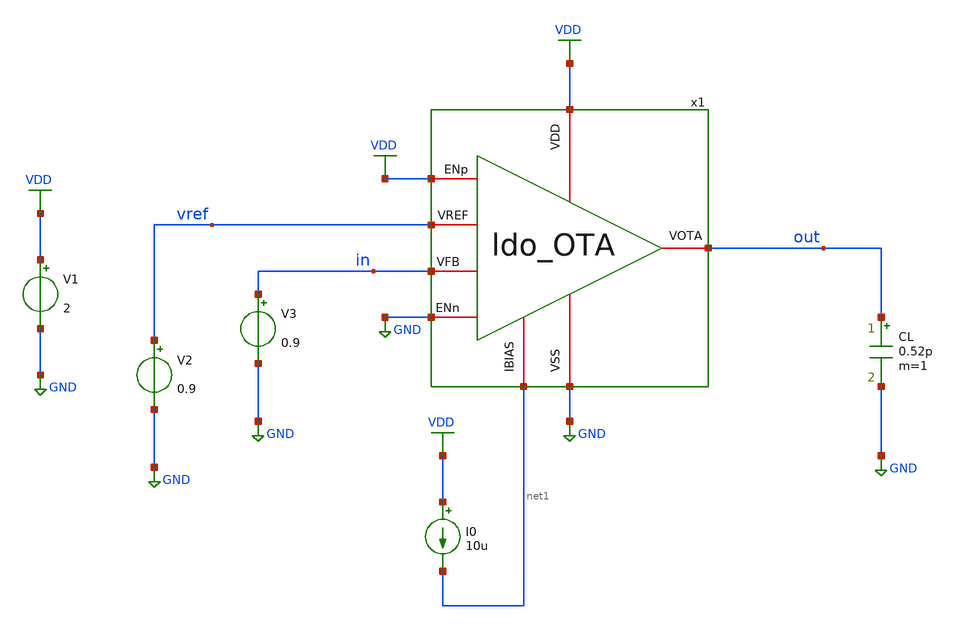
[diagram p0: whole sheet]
** sch_path: designs/libs/tb_ldo/tb_ldo_OTA_tran/tb_ldo_OTA_tran.sch
**.subckt tb_ldo_OTA_tran
V1 VDD GND 2
V2 vref GND 0.9
I0 VDD net1 10u
CL out GND 0.52p m=1
V3 in GND 0.9
x1 VDD vref in out net1 GND VDD GND ldo_OTA
**** begin user architecture code

.include $::180MCU_MODELS/design.ngspice
.lib $::180MCU_MODELS/sm141064.ngspice typical
.lib $::180MCU_MODELS/sm141064.ngspice cap_mim
.lib $::180MCU_MODELS/sm141064.ngspice moscap_typical
.lib $::180MCU_MODELS/sm141064.ngspice mimcap_typical
.lib $::180MCU_MODELS/sm141064.ngspice res_typical
* .lib $::180MCU_MODELS/sm141064.ngspice res_statistical
* ngspice commands




.control
save all

** Define input signal
let fsig = 1k
let tper = 1/fsig
let tfr = 0.01*tper
let ton = 0.5*tper-2*tfr

** Define transient params
let tstop = 2*tper
let tstep = 0.001*tper

** Set sources
alter @V3[PULSE] = [ 0.91 0.89 0 $&tfr $&tfr $&ton $&tper 0]

** Simulations
tran $&tstep $&tstop

** Plots
setplot tran1
let vout = v(out)
let vin = v(in)
plot vin
plot vout

write tb_ldo_OTA_tran.raw

.endc
* ngspice commands



**** end user architecture code
**.ends

* expanding   symbol:  libs/core_ldo/ldo_OTA/ldo_OTA.sym # of pins=8
** sym_path: designs/libs/core_ldo/ldo_OTA/ldo_OTA.sym
** sch_path: designs/libs/core_ldo/ldo_OTA/ldo_OTA.sch
.subckt ldo_OTA VDD VREF VFB VOTA IBIAS VSS ENp ENn
*.iopin VDD
*.iopin VSS
*.iopin VOTA
*.iopin VREF
*.iopin IBIAS
*.iopin VFB
*.ipin ENp
*.ipin ENn
XM3 Vbp1 Vbp1 VDD VDD pfet_05v0 L=1.00u W=5.50u nf=1 ad='int((nf+1)/2) * W/nf * 0.18u' as='int((nf+2)/2) * W/nf * 0.18u'
+ pd='2*int((nf+1)/2) * (W/nf + 0.18u)' ps='2*int((nf+2)/2) * (W/nf + 0.18u)' nrd='0.18u / W' nrs='0.18u / W'
+ sa=0 sb=0 sd=0 m=2
XM4 Vbp2 Vbp2 VDD VDD pfet_05v0 L=1.00u W=5.50u nf=1 ad='int((nf+1)/2) * W/nf * 0.18u' as='int((nf+2)/2) * W/nf * 0.18u'
+ pd='2*int((nf+1)/2) * (W/nf + 0.18u)' ps='2*int((nf+2)/2) * (W/nf + 0.18u)' nrd='0.18u / W' nrs='0.18u / W'
+ sa=0 sb=0 sd=0 m=2
XM5 Vbn2 Vbp1 VDD VDD pfet_05v0 L=1.00u W=5.50u nf=1 ad='int((nf+1)/2) * W/nf * 0.18u' as='int((nf+2)/2) * W/nf * 0.18u'
+ pd='2*int((nf+1)/2) * (W/nf + 0.18u)' ps='2*int((nf+2)/2) * (W/nf + 0.18u)' nrd='0.18u / W' nrs='0.18u / W'
+ sa=0 sb=0 sd=0 m=2
XM6 VOTA Vbp2 VDD VDD pfet_05v0 L=1.00u W=5.50u nf=1 ad='int((nf+1)/2) * W/nf * 0.18u' as='int((nf+2)/2) * W/nf * 0.18u'
+ pd='2*int((nf+1)/2) * (W/nf + 0.18u)' ps='2*int((nf+2)/2) * (W/nf + 0.18u)' nrd='0.18u / W' nrs='0.18u / W'
+ sa=0 sb=0 sd=0 m=6
XM9 Vbn1 Vbn1 VSS VSS nfet_05v0 L=1.00u W=3.00u nf=1 ad='int((nf+1)/2) * W/nf * 0.18u' as='int((nf+2)/2) * W/nf * 0.18u'
+ pd='2*int((nf+1)/2) * (W/nf + 0.18u)' ps='2*int((nf+2)/2) * (W/nf + 0.18u)' nrd='0.18u / W' nrs='0.18u / W'
+ sa=0 sb=0 sd=0 m=2
XM10 Vtail Vbn1 VSS VSS nfet_05v0 L=1.00u W=3.00u nf=1 ad='int((nf+1)/2) * W/nf * 0.18u' as='int((nf+2)/2) * W/nf * 0.18u'
+ pd='2*int((nf+1)/2) * (W/nf + 0.18u)' ps='2*int((nf+2)/2) * (W/nf + 0.18u)' nrd='0.18u / W' nrs='0.18u / W'
+ sa=0 sb=0 sd=0 m=2
XM7 Vbn2 Vbn2 VSS VSS nfet_05v0 L=1.00u W=1.25u nf=1 ad='int((nf+1)/2) * W/nf * 0.18u' as='int((nf+2)/2) * W/nf * 0.18u'
+ pd='2*int((nf+1)/2) * (W/nf + 0.18u)' ps='2*int((nf+2)/2) * (W/nf + 0.18u)' nrd='0.18u / W' nrs='0.18u / W'
+ sa=0 sb=0 sd=0 m=2
XM8 VOTA Vbn2 VSS VSS nfet_05v0 L=1.00u W=1.25u nf=1 ad='int((nf+1)/2) * W/nf * 0.18u' as='int((nf+2)/2) * W/nf * 0.18u'
+ pd='2*int((nf+1)/2) * (W/nf + 0.18u)' ps='2*int((nf+2)/2) * (W/nf + 0.18u)' nrd='0.18u / W' nrs='0.18u / W'
+ sa=0 sb=0 sd=0 m=6
XM1 Vbp1 VREF Vtail VSS nfet_05v0 L=0.60u W=5.00u nf=1 ad='int((nf+1)/2) * W/nf * 0.18u' as='int((nf+2)/2) * W/nf * 0.18u'
+ pd='2*int((nf+1)/2) * (W/nf + 0.18u)' ps='2*int((nf+2)/2) * (W/nf + 0.18u)' nrd='0.18u / W' nrs='0.18u / W'
+ sa=0 sb=0 sd=0 m=14
XM2 Vbp2 VFB Vtail VSS nfet_05v0 L=0.60u W=5.00u nf=1 ad='int((nf+1)/2) * W/nf * 0.18u' as='int((nf+2)/2) * W/nf * 0.18u'
+ pd='2*int((nf+1)/2) * (W/nf + 0.18u)' ps='2*int((nf+2)/2) * (W/nf + 0.18u)' nrd='0.18u / W' nrs='0.18u / W'
+ sa=0 sb=0 sd=0 m=14
XMpota_dummy_L[3] VDD VDD VDD VDD pfet_05v0 L=1.00u W=5.50u nf=1 ad='int((nf+1)/2) * W/nf * 0.18u' as='int((nf+2)/2) * W/nf * 0.18u'
+ pd='2*int((nf+1)/2) * (W/nf + 0.18u)' ps='2*int((nf+2)/2) * (W/nf + 0.18u)' nrd='0.18u / W' nrs='0.18u / W'
+ sa=0 sb=0 sd=0 m=1
XMpota_dummy_L[2] VDD VDD VDD VDD pfet_05v0 L=1.00u W=5.50u nf=1 ad='int((nf+1)/2) * W/nf * 0.18u' as='int((nf+2)/2) * W/nf * 0.18u'
+ pd='2*int((nf+1)/2) * (W/nf + 0.18u)' ps='2*int((nf+2)/2) * (W/nf + 0.18u)' nrd='0.18u / W' nrs='0.18u / W'
+ sa=0 sb=0 sd=0 m=1
XMpota_dummy_L[1] VDD VDD VDD VDD pfet_05v0 L=1.00u W=5.50u nf=1 ad='int((nf+1)/2) * W/nf * 0.18u' as='int((nf+2)/2) * W/nf * 0.18u'
+ pd='2*int((nf+1)/2) * (W/nf + 0.18u)' ps='2*int((nf+2)/2) * (W/nf + 0.18u)' nrd='0.18u / W' nrs='0.18u / W'
+ sa=0 sb=0 sd=0 m=1
XMpota_dummy_L[0] VDD VDD VDD VDD pfet_05v0 L=1.00u W=5.50u nf=1 ad='int((nf+1)/2) * W/nf * 0.18u' as='int((nf+2)/2) * W/nf * 0.18u'
+ pd='2*int((nf+1)/2) * (W/nf + 0.18u)' ps='2*int((nf+2)/2) * (W/nf + 0.18u)' nrd='0.18u / W' nrs='0.18u / W'
+ sa=0 sb=0 sd=0 m=1
XMpota_dummy_TB[15] VDD VDD VDD VDD pfet_05v0 L=1.00u W=5.50u nf=1 ad='int((nf+1)/2) * W/nf * 0.18u'
+ as='int((nf+2)/2) * W/nf * 0.18u' pd='2*int((nf+1)/2) * (W/nf + 0.18u)' ps='2*int((nf+2)/2) * (W/nf + 0.18u)'
+ nrd='0.18u / W' nrs='0.18u / W' sa=0 sb=0 sd=0 m=1
XMpota_dummy_TB[14] VDD VDD VDD VDD pfet_05v0 L=1.00u W=5.50u nf=1 ad='int((nf+1)/2) * W/nf * 0.18u'
+ as='int((nf+2)/2) * W/nf * 0.18u' pd='2*int((nf+1)/2) * (W/nf + 0.18u)' ps='2*int((nf+2)/2) * (W/nf + 0.18u)'
+ nrd='0.18u / W' nrs='0.18u / W' sa=0 sb=0 sd=0 m=1
XMpota_dummy_TB[13] VDD VDD VDD VDD pfet_05v0 L=1.00u W=5.50u nf=1 ad='int((nf+1)/2) * W/nf * 0.18u'
+ as='int((nf+2)/2) * W/nf * 0.18u' pd='2*int((nf+1)/2) * (W/nf + 0.18u)' ps='2*int((nf+2)/2) * (W/nf + 0.18u)'
+ nrd='0.18u / W' nrs='0.18u / W' sa=0 sb=0 sd=0 m=1
XMpota_dummy_TB[12] VDD VDD VDD VDD pfet_05v0 L=1.00u W=5.50u nf=1 ad='int((nf+1)/2) * W/nf * 0.18u'
+ as='int((nf+2)/2) * W/nf * 0.18u' pd='2*int((nf+1)/2) * (W/nf + 0.18u)' ps='2*int((nf+2)/2) * (W/nf + 0.18u)'
+ nrd='0.18u / W' nrs='0.18u / W' sa=0 sb=0 sd=0 m=1
XMpota_dummy_TB[11] VDD VDD VDD VDD pfet_05v0 L=1.00u W=5.50u nf=1 ad='int((nf+1)/2) * W/nf * 0.18u'
+ as='int((nf+2)/2) * W/nf * 0.18u' pd='2*int((nf+1)/2) * (W/nf + 0.18u)' ps='2*int((nf+2)/2) * (W/nf + 0.18u)'
+ nrd='0.18u / W' nrs='0.18u / W' sa=0 sb=0 sd=0 m=1
XMpota_dummy_TB[10] VDD VDD VDD VDD pfet_05v0 L=1.00u W=5.50u nf=1 ad='int((nf+1)/2) * W/nf * 0.18u'
+ as='int((nf+2)/2) * W/nf * 0.18u' pd='2*int((nf+1)/2) * (W/nf + 0.18u)' ps='2*int((nf+2)/2) * (W/nf + 0.18u)'
+ nrd='0.18u / W' nrs='0.18u / W' sa=0 sb=0 sd=0 m=1
XMpota_dummy_TB[9] VDD VDD VDD VDD pfet_05v0 L=1.00u W=5.50u nf=1 ad='int((nf+1)/2) * W/nf * 0.18u' as='int((nf+2)/2) * W/nf * 0.18u'
+ pd='2*int((nf+1)/2) * (W/nf + 0.18u)' ps='2*int((nf+2)/2) * (W/nf + 0.18u)' nrd='0.18u / W' nrs='0.18u / W'
+ sa=0 sb=0 sd=0 m=1
XMpota_dummy_TB[8] VDD VDD VDD VDD pfet_05v0 L=1.00u W=5.50u nf=1 ad='int((nf+1)/2) * W/nf * 0.18u' as='int((nf+2)/2) * W/nf * 0.18u'
+ pd='2*int((nf+1)/2) * (W/nf + 0.18u)' ps='2*int((nf+2)/2) * (W/nf + 0.18u)' nrd='0.18u / W' nrs='0.18u / W'
+ sa=0 sb=0 sd=0 m=1
XMpota_dummy_TB[7] VDD VDD VDD VDD pfet_05v0 L=1.00u W=5.50u nf=1 ad='int((nf+1)/2) * W/nf * 0.18u' as='int((nf+2)/2) * W/nf * 0.18u'
+ pd='2*int((nf+1)/2) * (W/nf + 0.18u)' ps='2*int((nf+2)/2) * (W/nf + 0.18u)' nrd='0.18u / W' nrs='0.18u / W'
+ sa=0 sb=0 sd=0 m=1
XMpota_dummy_TB[6] VDD VDD VDD VDD pfet_05v0 L=1.00u W=5.50u nf=1 ad='int((nf+1)/2) * W/nf * 0.18u' as='int((nf+2)/2) * W/nf * 0.18u'
+ pd='2*int((nf+1)/2) * (W/nf + 0.18u)' ps='2*int((nf+2)/2) * (W/nf + 0.18u)' nrd='0.18u / W' nrs='0.18u / W'
+ sa=0 sb=0 sd=0 m=1
XMpota_dummy_TB[5] VDD VDD VDD VDD pfet_05v0 L=1.00u W=5.50u nf=1 ad='int((nf+1)/2) * W/nf * 0.18u' as='int((nf+2)/2) * W/nf * 0.18u'
+ pd='2*int((nf+1)/2) * (W/nf + 0.18u)' ps='2*int((nf+2)/2) * (W/nf + 0.18u)' nrd='0.18u / W' nrs='0.18u / W'
+ sa=0 sb=0 sd=0 m=1
XMpota_dummy_TB[4] VDD VDD VDD VDD pfet_05v0 L=1.00u W=5.50u nf=1 ad='int((nf+1)/2) * W/nf * 0.18u' as='int((nf+2)/2) * W/nf * 0.18u'
+ pd='2*int((nf+1)/2) * (W/nf + 0.18u)' ps='2*int((nf+2)/2) * (W/nf + 0.18u)' nrd='0.18u / W' nrs='0.18u / W'
+ sa=0 sb=0 sd=0 m=1
XMpota_dummy_TB[3] VDD VDD VDD VDD pfet_05v0 L=1.00u W=5.50u nf=1 ad='int((nf+1)/2) * W/nf * 0.18u' as='int((nf+2)/2) * W/nf * 0.18u'
+ pd='2*int((nf+1)/2) * (W/nf + 0.18u)' ps='2*int((nf+2)/2) * (W/nf + 0.18u)' nrd='0.18u / W' nrs='0.18u / W'
+ sa=0 sb=0 sd=0 m=1
XMpota_dummy_TB[2] VDD VDD VDD VDD pfet_05v0 L=1.00u W=5.50u nf=1 ad='int((nf+1)/2) * W/nf * 0.18u' as='int((nf+2)/2) * W/nf * 0.18u'
+ pd='2*int((nf+1)/2) * (W/nf + 0.18u)' ps='2*int((nf+2)/2) * (W/nf + 0.18u)' nrd='0.18u / W' nrs='0.18u / W'
+ sa=0 sb=0 sd=0 m=1
XMpota_dummy_TB[1] VDD VDD VDD VDD pfet_05v0 L=1.00u W=5.50u nf=1 ad='int((nf+1)/2) * W/nf * 0.18u' as='int((nf+2)/2) * W/nf * 0.18u'
+ pd='2*int((nf+1)/2) * (W/nf + 0.18u)' ps='2*int((nf+2)/2) * (W/nf + 0.18u)' nrd='0.18u / W' nrs='0.18u / W'
+ sa=0 sb=0 sd=0 m=1
XMpota_dummy_TB[0] VDD VDD VDD VDD pfet_05v0 L=1.00u W=5.50u nf=1 ad='int((nf+1)/2) * W/nf * 0.18u' as='int((nf+2)/2) * W/nf * 0.18u'
+ pd='2*int((nf+1)/2) * (W/nf + 0.18u)' ps='2*int((nf+2)/2) * (W/nf + 0.18u)' nrd='0.18u / W' nrs='0.18u / W'
+ sa=0 sb=0 sd=0 m=1
XMndiff_dummy_L[7] VSS VSS VSS VSS nfet_05v0 L=0.60u W=5.00u nf=1 ad='int((nf+1)/2) * W/nf * 0.18u' as='int((nf+2)/2) * W/nf * 0.18u'
+ pd='2*int((nf+1)/2) * (W/nf + 0.18u)' ps='2*int((nf+2)/2) * (W/nf + 0.18u)' nrd='0.18u / W' nrs='0.18u / W'
+ sa=0 sb=0 sd=0 m=1
XMndiff_dummy_L[6] VSS VSS VSS VSS nfet_05v0 L=0.60u W=5.00u nf=1 ad='int((nf+1)/2) * W/nf * 0.18u' as='int((nf+2)/2) * W/nf * 0.18u'
+ pd='2*int((nf+1)/2) * (W/nf + 0.18u)' ps='2*int((nf+2)/2) * (W/nf + 0.18u)' nrd='0.18u / W' nrs='0.18u / W'
+ sa=0 sb=0 sd=0 m=1
XMndiff_dummy_L[5] VSS VSS VSS VSS nfet_05v0 L=0.60u W=5.00u nf=1 ad='int((nf+1)/2) * W/nf * 0.18u' as='int((nf+2)/2) * W/nf * 0.18u'
+ pd='2*int((nf+1)/2) * (W/nf + 0.18u)' ps='2*int((nf+2)/2) * (W/nf + 0.18u)' nrd='0.18u / W' nrs='0.18u / W'
+ sa=0 sb=0 sd=0 m=1
XMndiff_dummy_L[4] VSS VSS VSS VSS nfet_05v0 L=0.60u W=5.00u nf=1 ad='int((nf+1)/2) * W/nf * 0.18u' as='int((nf+2)/2) * W/nf * 0.18u'
+ pd='2*int((nf+1)/2) * (W/nf + 0.18u)' ps='2*int((nf+2)/2) * (W/nf + 0.18u)' nrd='0.18u / W' nrs='0.18u / W'
+ sa=0 sb=0 sd=0 m=1
XMndiff_dummy_L[3] VSS VSS VSS VSS nfet_05v0 L=0.60u W=5.00u nf=1 ad='int((nf+1)/2) * W/nf * 0.18u' as='int((nf+2)/2) * W/nf * 0.18u'
+ pd='2*int((nf+1)/2) * (W/nf + 0.18u)' ps='2*int((nf+2)/2) * (W/nf + 0.18u)' nrd='0.18u / W' nrs='0.18u / W'
+ sa=0 sb=0 sd=0 m=1
XMndiff_dummy_L[2] VSS VSS VSS VSS nfet_05v0 L=0.60u W=5.00u nf=1 ad='int((nf+1)/2) * W/nf * 0.18u' as='int((nf+2)/2) * W/nf * 0.18u'
+ pd='2*int((nf+1)/2) * (W/nf + 0.18u)' ps='2*int((nf+2)/2) * (W/nf + 0.18u)' nrd='0.18u / W' nrs='0.18u / W'
+ sa=0 sb=0 sd=0 m=1
XMndiff_dummy_L[1] VSS VSS VSS VSS nfet_05v0 L=0.60u W=5.00u nf=1 ad='int((nf+1)/2) * W/nf * 0.18u' as='int((nf+2)/2) * W/nf * 0.18u'
+ pd='2*int((nf+1)/2) * (W/nf + 0.18u)' ps='2*int((nf+2)/2) * (W/nf + 0.18u)' nrd='0.18u / W' nrs='0.18u / W'
+ sa=0 sb=0 sd=0 m=1
XMndiff_dummy_L[0] VSS VSS VSS VSS nfet_05v0 L=0.60u W=5.00u nf=1 ad='int((nf+1)/2) * W/nf * 0.18u' as='int((nf+2)/2) * W/nf * 0.18u'
+ pd='2*int((nf+1)/2) * (W/nf + 0.18u)' ps='2*int((nf+2)/2) * (W/nf + 0.18u)' nrd='0.18u / W' nrs='0.18u / W'
+ sa=0 sb=0 sd=0 m=1
XMndiff_dummy_TB[17] VSS VSS VSS VSS nfet_05v0 L=0.60u W=5.00u nf=1 ad='int((nf+1)/2) * W/nf * 0.18u'
+ as='int((nf+2)/2) * W/nf * 0.18u' pd='2*int((nf+1)/2) * (W/nf + 0.18u)' ps='2*int((nf+2)/2) * (W/nf + 0.18u)'
+ nrd='0.18u / W' nrs='0.18u / W' sa=0 sb=0 sd=0 m=1
XMndiff_dummy_TB[16] VSS VSS VSS VSS nfet_05v0 L=0.60u W=5.00u nf=1 ad='int((nf+1)/2) * W/nf * 0.18u'
+ as='int((nf+2)/2) * W/nf * 0.18u' pd='2*int((nf+1)/2) * (W/nf + 0.18u)' ps='2*int((nf+2)/2) * (W/nf + 0.18u)'
+ nrd='0.18u / W' nrs='0.18u / W' sa=0 sb=0 sd=0 m=1
XMndiff_dummy_TB[15] VSS VSS VSS VSS nfet_05v0 L=0.60u W=5.00u nf=1 ad='int((nf+1)/2) * W/nf * 0.18u'
+ as='int((nf+2)/2) * W/nf * 0.18u' pd='2*int((nf+1)/2) * (W/nf + 0.18u)' ps='2*int((nf+2)/2) * (W/nf + 0.18u)'
+ nrd='0.18u / W' nrs='0.18u / W' sa=0 sb=0 sd=0 m=1
XMndiff_dummy_TB[14] VSS VSS VSS VSS nfet_05v0 L=0.60u W=5.00u nf=1 ad='int((nf+1)/2) * W/nf * 0.18u'
+ as='int((nf+2)/2) * W/nf * 0.18u' pd='2*int((nf+1)/2) * (W/nf + 0.18u)' ps='2*int((nf+2)/2) * (W/nf + 0.18u)'
+ nrd='0.18u / W' nrs='0.18u / W' sa=0 sb=0 sd=0 m=1
XMndiff_dummy_TB[13] VSS VSS VSS VSS nfet_05v0 L=0.60u W=5.00u nf=1 ad='int((nf+1)/2) * W/nf * 0.18u'
+ as='int((nf+2)/2) * W/nf * 0.18u' pd='2*int((nf+1)/2) * (W/nf + 0.18u)' ps='2*int((nf+2)/2) * (W/nf + 0.18u)'
+ nrd='0.18u / W' nrs='0.18u / W' sa=0 sb=0 sd=0 m=1
XMndiff_dummy_TB[12] VSS VSS VSS VSS nfet_05v0 L=0.60u W=5.00u nf=1 ad='int((nf+1)/2) * W/nf * 0.18u'
+ as='int((nf+2)/2) * W/nf * 0.18u' pd='2*int((nf+1)/2) * (W/nf + 0.18u)' ps='2*int((nf+2)/2) * (W/nf + 0.18u)'
+ nrd='0.18u / W' nrs='0.18u / W' sa=0 sb=0 sd=0 m=1
XMndiff_dummy_TB[11] VSS VSS VSS VSS nfet_05v0 L=0.60u W=5.00u nf=1 ad='int((nf+1)/2) * W/nf * 0.18u'
+ as='int((nf+2)/2) * W/nf * 0.18u' pd='2*int((nf+1)/2) * (W/nf + 0.18u)' ps='2*int((nf+2)/2) * (W/nf + 0.18u)'
+ nrd='0.18u / W' nrs='0.18u / W' sa=0 sb=0 sd=0 m=1
XMndiff_dummy_TB[10] VSS VSS VSS VSS nfet_05v0 L=0.60u W=5.00u nf=1 ad='int((nf+1)/2) * W/nf * 0.18u'
+ as='int((nf+2)/2) * W/nf * 0.18u' pd='2*int((nf+1)/2) * (W/nf + 0.18u)' ps='2*int((nf+2)/2) * (W/nf + 0.18u)'
+ nrd='0.18u / W' nrs='0.18u / W' sa=0 sb=0 sd=0 m=1
XMndiff_dummy_TB[9] VSS VSS VSS VSS nfet_05v0 L=0.60u W=5.00u nf=1 ad='int((nf+1)/2) * W/nf * 0.18u'
+ as='int((nf+2)/2) * W/nf * 0.18u' pd='2*int((nf+1)/2) * (W/nf + 0.18u)' ps='2*int((nf+2)/2) * (W/nf + 0.18u)'
+ nrd='0.18u / W' nrs='0.18u / W' sa=0 sb=0 sd=0 m=1
XMndiff_dummy_TB[8] VSS VSS VSS VSS nfet_05v0 L=0.60u W=5.00u nf=1 ad='int((nf+1)/2) * W/nf * 0.18u'
+ as='int((nf+2)/2) * W/nf * 0.18u' pd='2*int((nf+1)/2) * (W/nf + 0.18u)' ps='2*int((nf+2)/2) * (W/nf + 0.18u)'
+ nrd='0.18u / W' nrs='0.18u / W' sa=0 sb=0 sd=0 m=1
XMndiff_dummy_TB[7] VSS VSS VSS VSS nfet_05v0 L=0.60u W=5.00u nf=1 ad='int((nf+1)/2) * W/nf * 0.18u'
+ as='int((nf+2)/2) * W/nf * 0.18u' pd='2*int((nf+1)/2) * (W/nf + 0.18u)' ps='2*int((nf+2)/2) * (W/nf + 0.18u)'
+ nrd='0.18u / W' nrs='0.18u / W' sa=0 sb=0 sd=0 m=1
XMndiff_dummy_TB[6] VSS VSS VSS VSS nfet_05v0 L=0.60u W=5.00u nf=1 ad='int((nf+1)/2) * W/nf * 0.18u'
+ as='int((nf+2)/2) * W/nf * 0.18u' pd='2*int((nf+1)/2) * (W/nf + 0.18u)' ps='2*int((nf+2)/2) * (W/nf + 0.18u)'
+ nrd='0.18u / W' nrs='0.18u / W' sa=0 sb=0 sd=0 m=1
XMndiff_dummy_TB[5] VSS VSS VSS VSS nfet_05v0 L=0.60u W=5.00u nf=1 ad='int((nf+1)/2) * W/nf * 0.18u'
+ as='int((nf+2)/2) * W/nf * 0.18u' pd='2*int((nf+1)/2) * (W/nf + 0.18u)' ps='2*int((nf+2)/2) * (W/nf + 0.18u)'
+ nrd='0.18u / W' nrs='0.18u / W' sa=0 sb=0 sd=0 m=1
XMndiff_dummy_TB[4] VSS VSS VSS VSS nfet_05v0 L=0.60u W=5.00u nf=1 ad='int((nf+1)/2) * W/nf * 0.18u'
+ as='int((nf+2)/2) * W/nf * 0.18u' pd='2*int((nf+1)/2) * (W/nf + 0.18u)' ps='2*int((nf+2)/2) * (W/nf + 0.18u)'
+ nrd='0.18u / W' nrs='0.18u / W' sa=0 sb=0 sd=0 m=1
XMndiff_dummy_TB[3] VSS VSS VSS VSS nfet_05v0 L=0.60u W=5.00u nf=1 ad='int((nf+1)/2) * W/nf * 0.18u'
+ as='int((nf+2)/2) * W/nf * 0.18u' pd='2*int((nf+1)/2) * (W/nf + 0.18u)' ps='2*int((nf+2)/2) * (W/nf + 0.18u)'
+ nrd='0.18u / W' nrs='0.18u / W' sa=0 sb=0 sd=0 m=1
XMndiff_dummy_TB[2] VSS VSS VSS VSS nfet_05v0 L=0.60u W=5.00u nf=1 ad='int((nf+1)/2) * W/nf * 0.18u'
+ as='int((nf+2)/2) * W/nf * 0.18u' pd='2*int((nf+1)/2) * (W/nf + 0.18u)' ps='2*int((nf+2)/2) * (W/nf + 0.18u)'
+ nrd='0.18u / W' nrs='0.18u / W' sa=0 sb=0 sd=0 m=1
XMndiff_dummy_TB[1] VSS VSS VSS VSS nfet_05v0 L=0.60u W=5.00u nf=1 ad='int((nf+1)/2) * W/nf * 0.18u'
+ as='int((nf+2)/2) * W/nf * 0.18u' pd='2*int((nf+1)/2) * (W/nf + 0.18u)' ps='2*int((nf+2)/2) * (W/nf + 0.18u)'
+ nrd='0.18u / W' nrs='0.18u / W' sa=0 sb=0 sd=0 m=1
XMndiff_dummy_TB[0] VSS VSS VSS VSS nfet_05v0 L=0.60u W=5.00u nf=1 ad='int((nf+1)/2) * W/nf * 0.18u'
+ as='int((nf+2)/2) * W/nf * 0.18u' pd='2*int((nf+1)/2) * (W/nf + 0.18u)' ps='2*int((nf+2)/2) * (W/nf + 0.18u)'
+ nrd='0.18u / W' nrs='0.18u / W' sa=0 sb=0 sd=0 m=1
XMnota_dummy_L[3] VSS VSS VSS VSS nfet_05v0 L=1.00u W=1.25u nf=1 ad='int((nf+1)/2) * W/nf * 0.18u' as='int((nf+2)/2) * W/nf * 0.18u'
+ pd='2*int((nf+1)/2) * (W/nf + 0.18u)' ps='2*int((nf+2)/2) * (W/nf + 0.18u)' nrd='0.18u / W' nrs='0.18u / W'
+ sa=0 sb=0 sd=0 m=1
XMnota_dummy_L[2] VSS VSS VSS VSS nfet_05v0 L=1.00u W=1.25u nf=1 ad='int((nf+1)/2) * W/nf * 0.18u' as='int((nf+2)/2) * W/nf * 0.18u'
+ pd='2*int((nf+1)/2) * (W/nf + 0.18u)' ps='2*int((nf+2)/2) * (W/nf + 0.18u)' nrd='0.18u / W' nrs='0.18u / W'
+ sa=0 sb=0 sd=0 m=1
XMnota_dummy_L[1] VSS VSS VSS VSS nfet_05v0 L=1.00u W=1.25u nf=1 ad='int((nf+1)/2) * W/nf * 0.18u' as='int((nf+2)/2) * W/nf * 0.18u'
+ pd='2*int((nf+1)/2) * (W/nf + 0.18u)' ps='2*int((nf+2)/2) * (W/nf + 0.18u)' nrd='0.18u / W' nrs='0.18u / W'
+ sa=0 sb=0 sd=0 m=1
XMnota_dummy_L[0] VSS VSS VSS VSS nfet_05v0 L=1.00u W=1.25u nf=1 ad='int((nf+1)/2) * W/nf * 0.18u' as='int((nf+2)/2) * W/nf * 0.18u'
+ pd='2*int((nf+1)/2) * (W/nf + 0.18u)' ps='2*int((nf+2)/2) * (W/nf + 0.18u)' nrd='0.18u / W' nrs='0.18u / W'
+ sa=0 sb=0 sd=0 m=1
XMnota_dummy_TB[11] VSS VSS VSS VSS nfet_05v0 L=1.00u W=1.25u nf=1 ad='int((nf+1)/2) * W/nf * 0.18u'
+ as='int((nf+2)/2) * W/nf * 0.18u' pd='2*int((nf+1)/2) * (W/nf + 0.18u)' ps='2*int((nf+2)/2) * (W/nf + 0.18u)'
+ nrd='0.18u / W' nrs='0.18u / W' sa=0 sb=0 sd=0 m=1
XMnota_dummy_TB[10] VSS VSS VSS VSS nfet_05v0 L=1.00u W=1.25u nf=1 ad='int((nf+1)/2) * W/nf * 0.18u'
+ as='int((nf+2)/2) * W/nf * 0.18u' pd='2*int((nf+1)/2) * (W/nf + 0.18u)' ps='2*int((nf+2)/2) * (W/nf + 0.18u)'
+ nrd='0.18u / W' nrs='0.18u / W' sa=0 sb=0 sd=0 m=1
XMnota_dummy_TB[9] VSS VSS VSS VSS nfet_05v0 L=1.00u W=1.25u nf=1 ad='int((nf+1)/2) * W/nf * 0.18u' as='int((nf+2)/2) * W/nf * 0.18u'
+ pd='2*int((nf+1)/2) * (W/nf + 0.18u)' ps='2*int((nf+2)/2) * (W/nf + 0.18u)' nrd='0.18u / W' nrs='0.18u / W'
+ sa=0 sb=0 sd=0 m=1
XMnota_dummy_TB[8] VSS VSS VSS VSS nfet_05v0 L=1.00u W=1.25u nf=1 ad='int((nf+1)/2) * W/nf * 0.18u' as='int((nf+2)/2) * W/nf * 0.18u'
+ pd='2*int((nf+1)/2) * (W/nf + 0.18u)' ps='2*int((nf+2)/2) * (W/nf + 0.18u)' nrd='0.18u / W' nrs='0.18u / W'
+ sa=0 sb=0 sd=0 m=1
XMnota_dummy_TB[7] VSS VSS VSS VSS nfet_05v0 L=1.00u W=1.25u nf=1 ad='int((nf+1)/2) * W/nf * 0.18u' as='int((nf+2)/2) * W/nf * 0.18u'
+ pd='2*int((nf+1)/2) * (W/nf + 0.18u)' ps='2*int((nf+2)/2) * (W/nf + 0.18u)' nrd='0.18u / W' nrs='0.18u / W'
+ sa=0 sb=0 sd=0 m=1
XMnota_dummy_TB[6] VSS VSS VSS VSS nfet_05v0 L=1.00u W=1.25u nf=1 ad='int((nf+1)/2) * W/nf * 0.18u' as='int((nf+2)/2) * W/nf * 0.18u'
+ pd='2*int((nf+1)/2) * (W/nf + 0.18u)' ps='2*int((nf+2)/2) * (W/nf + 0.18u)' nrd='0.18u / W' nrs='0.18u / W'
+ sa=0 sb=0 sd=0 m=1
XMnota_dummy_TB[5] VSS VSS VSS VSS nfet_05v0 L=1.00u W=1.25u nf=1 ad='int((nf+1)/2) * W/nf * 0.18u' as='int((nf+2)/2) * W/nf * 0.18u'
+ pd='2*int((nf+1)/2) * (W/nf + 0.18u)' ps='2*int((nf+2)/2) * (W/nf + 0.18u)' nrd='0.18u / W' nrs='0.18u / W'
+ sa=0 sb=0 sd=0 m=1
XMnota_dummy_TB[4] VSS VSS VSS VSS nfet_05v0 L=1.00u W=1.25u nf=1 ad='int((nf+1)/2) * W/nf * 0.18u' as='int((nf+2)/2) * W/nf * 0.18u'
+ pd='2*int((nf+1)/2) * (W/nf + 0.18u)' ps='2*int((nf+2)/2) * (W/nf + 0.18u)' nrd='0.18u / W' nrs='0.18u / W'
+ sa=0 sb=0 sd=0 m=1
XMnota_dummy_TB[3] VSS VSS VSS VSS nfet_05v0 L=1.00u W=1.25u nf=1 ad='int((nf+1)/2) * W/nf * 0.18u' as='int((nf+2)/2) * W/nf * 0.18u'
+ pd='2*int((nf+1)/2) * (W/nf + 0.18u)' ps='2*int((nf+2)/2) * (W/nf + 0.18u)' nrd='0.18u / W' nrs='0.18u / W'
+ sa=0 sb=0 sd=0 m=1
XMnota_dummy_TB[2] VSS VSS VSS VSS nfet_05v0 L=1.00u W=1.25u nf=1 ad='int((nf+1)/2) * W/nf * 0.18u' as='int((nf+2)/2) * W/nf * 0.18u'
+ pd='2*int((nf+1)/2) * (W/nf + 0.18u)' ps='2*int((nf+2)/2) * (W/nf + 0.18u)' nrd='0.18u / W' nrs='0.18u / W'
+ sa=0 sb=0 sd=0 m=1
XMnota_dummy_TB[1] VSS VSS VSS VSS nfet_05v0 L=1.00u W=1.25u nf=1 ad='int((nf+1)/2) * W/nf * 0.18u' as='int((nf+2)/2) * W/nf * 0.18u'
+ pd='2*int((nf+1)/2) * (W/nf + 0.18u)' ps='2*int((nf+2)/2) * (W/nf + 0.18u)' nrd='0.18u / W' nrs='0.18u / W'
+ sa=0 sb=0 sd=0 m=1
XMnota_dummy_TB[0] VSS VSS VSS VSS nfet_05v0 L=1.00u W=1.25u nf=1 ad='int((nf+1)/2) * W/nf * 0.18u' as='int((nf+2)/2) * W/nf * 0.18u'
+ pd='2*int((nf+1)/2) * (W/nf + 0.18u)' ps='2*int((nf+2)/2) * (W/nf + 0.18u)' nrd='0.18u / W' nrs='0.18u / W'
+ sa=0 sb=0 sd=0 m=1
XMnbias_dummy_L[3] VSS VSS VSS VSS nfet_05v0 L=1.00u W=3.00u nf=1 ad='int((nf+1)/2) * W/nf * 0.18u' as='int((nf+2)/2) * W/nf * 0.18u'
+ pd='2*int((nf+1)/2) * (W/nf + 0.18u)' ps='2*int((nf+2)/2) * (W/nf + 0.18u)' nrd='0.18u / W' nrs='0.18u / W'
+ sa=0 sb=0 sd=0 m=1
XMnbias_dummy_L[2] VSS VSS VSS VSS nfet_05v0 L=1.00u W=3.00u nf=1 ad='int((nf+1)/2) * W/nf * 0.18u' as='int((nf+2)/2) * W/nf * 0.18u'
+ pd='2*int((nf+1)/2) * (W/nf + 0.18u)' ps='2*int((nf+2)/2) * (W/nf + 0.18u)' nrd='0.18u / W' nrs='0.18u / W'
+ sa=0 sb=0 sd=0 m=1
XMnbias_dummy_L[1] VSS VSS VSS VSS nfet_05v0 L=1.00u W=3.00u nf=1 ad='int((nf+1)/2) * W/nf * 0.18u' as='int((nf+2)/2) * W/nf * 0.18u'
+ pd='2*int((nf+1)/2) * (W/nf + 0.18u)' ps='2*int((nf+2)/2) * (W/nf + 0.18u)' nrd='0.18u / W' nrs='0.18u / W'
+ sa=0 sb=0 sd=0 m=1
XMnbias_dummy_L[0] VSS VSS VSS VSS nfet_05v0 L=1.00u W=3.00u nf=1 ad='int((nf+1)/2) * W/nf * 0.18u' as='int((nf+2)/2) * W/nf * 0.18u'
+ pd='2*int((nf+1)/2) * (W/nf + 0.18u)' ps='2*int((nf+2)/2) * (W/nf + 0.18u)' nrd='0.18u / W' nrs='0.18u / W'
+ sa=0 sb=0 sd=0 m=1
XMnbias_dummy_TB[7] VSS VSS VSS VSS nfet_05v0 L=1.00u W=3.00u nf=1 ad='int((nf+1)/2) * W/nf * 0.18u'
+ as='int((nf+2)/2) * W/nf * 0.18u' pd='2*int((nf+1)/2) * (W/nf + 0.18u)' ps='2*int((nf+2)/2) * (W/nf + 0.18u)'
+ nrd='0.18u / W' nrs='0.18u / W' sa=0 sb=0 sd=0 m=1
XMnbias_dummy_TB[6] VSS VSS VSS VSS nfet_05v0 L=1.00u W=3.00u nf=1 ad='int((nf+1)/2) * W/nf * 0.18u'
+ as='int((nf+2)/2) * W/nf * 0.18u' pd='2*int((nf+1)/2) * (W/nf + 0.18u)' ps='2*int((nf+2)/2) * (W/nf + 0.18u)'
+ nrd='0.18u / W' nrs='0.18u / W' sa=0 sb=0 sd=0 m=1
XMnbias_dummy_TB[5] VSS VSS VSS VSS nfet_05v0 L=1.00u W=3.00u nf=1 ad='int((nf+1)/2) * W/nf * 0.18u'
+ as='int((nf+2)/2) * W/nf * 0.18u' pd='2*int((nf+1)/2) * (W/nf + 0.18u)' ps='2*int((nf+2)/2) * (W/nf + 0.18u)'
+ nrd='0.18u / W' nrs='0.18u / W' sa=0 sb=0 sd=0 m=1
XMnbias_dummy_TB[4] VSS VSS VSS VSS nfet_05v0 L=1.00u W=3.00u nf=1 ad='int((nf+1)/2) * W/nf * 0.18u'
+ as='int((nf+2)/2) * W/nf * 0.18u' pd='2*int((nf+1)/2) * (W/nf + 0.18u)' ps='2*int((nf+2)/2) * (W/nf + 0.18u)'
+ nrd='0.18u / W' nrs='0.18u / W' sa=0 sb=0 sd=0 m=1
XMnbias_dummy_TB[3] VSS VSS VSS VSS nfet_05v0 L=1.00u W=3.00u nf=1 ad='int((nf+1)/2) * W/nf * 0.18u'
+ as='int((nf+2)/2) * W/nf * 0.18u' pd='2*int((nf+1)/2) * (W/nf + 0.18u)' ps='2*int((nf+2)/2) * (W/nf + 0.18u)'
+ nrd='0.18u / W' nrs='0.18u / W' sa=0 sb=0 sd=0 m=1
XMnbias_dummy_TB[2] VSS VSS VSS VSS nfet_05v0 L=1.00u W=3.00u nf=1 ad='int((nf+1)/2) * W/nf * 0.18u'
+ as='int((nf+2)/2) * W/nf * 0.18u' pd='2*int((nf+1)/2) * (W/nf + 0.18u)' ps='2*int((nf+2)/2) * (W/nf + 0.18u)'
+ nrd='0.18u / W' nrs='0.18u / W' sa=0 sb=0 sd=0 m=1
XMnbias_dummy_TB[1] VSS VSS VSS VSS nfet_05v0 L=1.00u W=3.00u nf=1 ad='int((nf+1)/2) * W/nf * 0.18u'
+ as='int((nf+2)/2) * W/nf * 0.18u' pd='2*int((nf+1)/2) * (W/nf + 0.18u)' ps='2*int((nf+2)/2) * (W/nf + 0.18u)'
+ nrd='0.18u / W' nrs='0.18u / W' sa=0 sb=0 sd=0 m=1
XMnbias_dummy_TB[0] VSS VSS VSS VSS nfet_05v0 L=1.00u W=3.00u nf=1 ad='int((nf+1)/2) * W/nf * 0.18u'
+ as='int((nf+2)/2) * W/nf * 0.18u' pd='2*int((nf+1)/2) * (W/nf + 0.18u)' ps='2*int((nf+2)/2) * (W/nf + 0.18u)'
+ nrd='0.18u / W' nrs='0.18u / W' sa=0 sb=0 sd=0 m=1
XMpenota1 Vbp2 ENp VDD VDD pfet_05v0 L=0.5u W=2u nf=1 ad='int((nf+1)/2) * W/nf * 0.18u' as='int((nf+2)/2) * W/nf * 0.18u'
+ pd='2*int((nf+1)/2) * (W/nf + 0.18u)' ps='2*int((nf+2)/2) * (W/nf + 0.18u)' nrd='0.18u / W' nrs='0.18u / W'
+ sa=0 sb=0 sd=0 m=1
XMpenota2 Vbp1 ENp VDD VDD pfet_05v0 L=0.5u W=2u nf=1 ad='int((nf+1)/2) * W/nf * 0.18u' as='int((nf+2)/2) * W/nf * 0.18u'
+ pd='2*int((nf+1)/2) * (W/nf + 0.18u)' ps='2*int((nf+2)/2) * (W/nf + 0.18u)' nrd='0.18u / W' nrs='0.18u / W'
+ sa=0 sb=0 sd=0 m=1
XMnenota1 Vbn2 ENn VSS VSS nfet_05v0 L=0.6u W=2u nf=1 ad='int((nf+1)/2) * W/nf * 0.18u' as='int((nf+2)/2) * W/nf * 0.18u'
+ pd='2*int((nf+1)/2) * (W/nf + 0.18u)' ps='2*int((nf+2)/2) * (W/nf + 0.18u)' nrd='0.18u / W' nrs='0.18u / W'
+ sa=0 sb=0 sd=0 m=1
XMnenota2 Vbn1 ENn VSS VSS nfet_05v0 L=0.6u W=2u nf=1 ad='int((nf+1)/2) * W/nf * 0.18u' as='int((nf+2)/2) * W/nf * 0.18u'
+ pd='2*int((nf+1)/2) * (W/nf + 0.18u)' ps='2*int((nf+2)/2) * (W/nf + 0.18u)' nrd='0.18u / W' nrs='0.18u / W'
+ sa=0 sb=0 sd=0 m=1
XMnenota3 IBIAS ENp Vbn1 VSS nfet_05v0 L=0.6u W=2u nf=1 ad='int((nf+1)/2) * W/nf * 0.18u' as='int((nf+2)/2) * W/nf * 0.18u'
+ pd='2*int((nf+1)/2) * (W/nf + 0.18u)' ps='2*int((nf+2)/2) * (W/nf + 0.18u)' nrd='0.18u / W' nrs='0.18u / W'
+ sa=0 sb=0 sd=0 m=1
.ends

.GLOBAL GND
.GLOBAL VDD
.end
